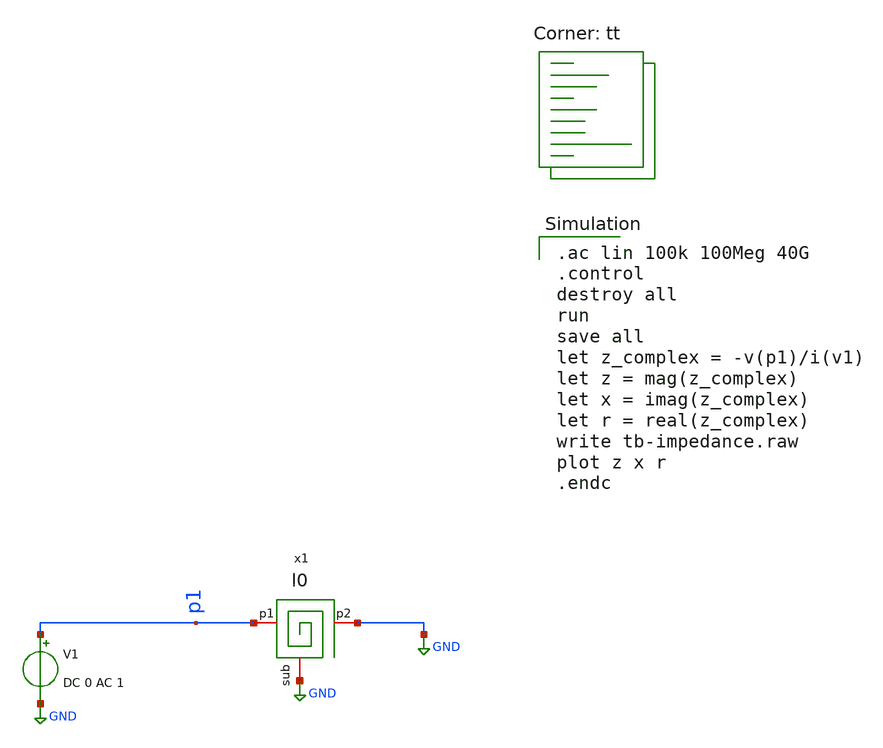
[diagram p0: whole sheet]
** sch_path: examples/sq_1nH_2.5GHz/xschem/tb-ind.sch
**.subckt tb-ind
V1 p1 GND DC 0 AC 1
x1 p1 GND GND l0
**** begin user architecture code

.ac lin 100k 100Meg 40G
.control
destroy all
run
save all
let z_complex = -v(p1)/i(v1)
let z = mag(z_complex)
let x = imag(z_complex)
let r = real(z_complex)
write tb-impedance.raw
plot z x r
.endc

.lib $::SKYWATER_MODELS/sky130.lib.spice tt
**** end user architecture code
**.ends

* expanding   symbol:  /foss/designs/asitic-example/examples/sq_1nH_2.5GHz/xschem/l0.sym # of pins=3
** sym_path: examples/sq_1nH_2.5GHz/xschem/l0.sym
** sch_path: examples/sq_1nH_2.5GHz/xschem/l0.sch
.subckt l0 p1 p2 sub
*.iopin sub
*.iopin p1
*.iopin p2
R net2 p2 2.857 m=1
L p1 net2 1.006n m=1
Rs1 net1 sub 27.37 m=1
Cs1 p1 net1 33.97f m=1
Cs2 p2 net3 36.78f m=1
Rs2 net3 sub -9 m=1
.ends

.GLOBAL GND
.end
